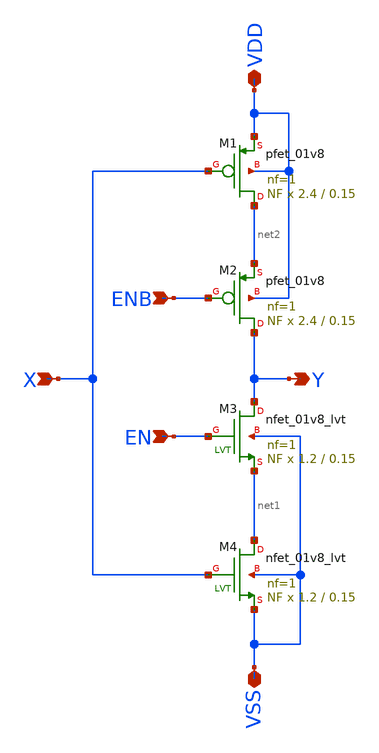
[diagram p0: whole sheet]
** sch_path: xschem_lib/sylee21/tinv.sch
**.subckt tinv X ENB EN Y VDD VSS
*.ipin X
*.ipin ENB
*.ipin EN
*.opin Y
*.iopin VDD
*.iopin VSS
XM1 net2 X VDD VDD sky130_fd_pr__pfet_01v8 L=0.15 W=2.4 nf=1 ad='int((nf+1)/2) * W/nf * 0.29' as='int((nf+2)/2) * W/nf * 0.29'
+ pd='2*int((nf+1)/2) * (W/nf + 0.29)' ps='2*int((nf+2)/2) * (W/nf + 0.29)' nrd='0.29 / W' nrs='0.29 / W'
+ sa=0 sb=0 sd=0 mult=NF m=NF
XM2 Y ENB net2 VDD sky130_fd_pr__pfet_01v8 L=0.15 W=2.4 nf=1 ad='int((nf+1)/2) * W/nf * 0.29' as='int((nf+2)/2) * W/nf * 0.29'
+ pd='2*int((nf+1)/2) * (W/nf + 0.29)' ps='2*int((nf+2)/2) * (W/nf + 0.29)' nrd='0.29 / W' nrs='0.29 / W'
+ sa=0 sb=0 sd=0 mult=NF m=NF
XM3 Y EN net1 VSS sky130_fd_pr__nfet_01v8_lvt L=0.15 W=1.2 nf=1 ad='int((nf+1)/2) * W/nf * 0.29' as='int((nf+2)/2) * W/nf * 0.29'
+ pd='2*int((nf+1)/2) * (W/nf + 0.29)' ps='2*int((nf+2)/2) * (W/nf + 0.29)' nrd='0.29 / W' nrs='0.29 / W'
+ sa=0 sb=0 sd=0 mult=NF m=NF
XM4 net1 X VSS VSS sky130_fd_pr__nfet_01v8_lvt L=0.15 W=1.2 nf=1 ad='int((nf+1)/2) * W/nf * 0.29' as='int((nf+2)/2) * W/nf * 0.29'
+ pd='2*int((nf+1)/2) * (W/nf + 0.29)' ps='2*int((nf+2)/2) * (W/nf + 0.29)' nrd='0.29 / W' nrs='0.29 / W'
+ sa=0 sb=0 sd=0 mult=NF m=NF
**.ends
.end
